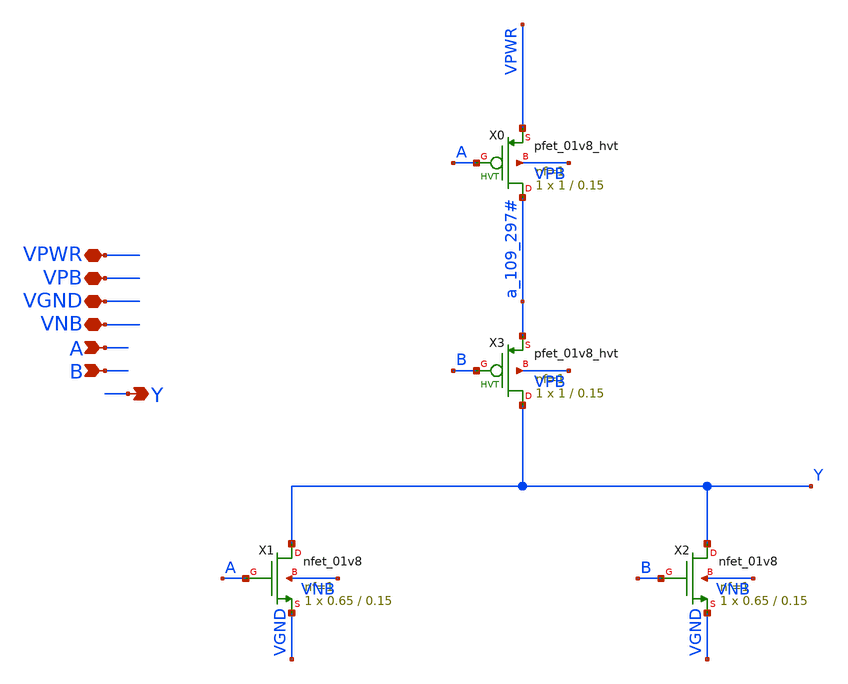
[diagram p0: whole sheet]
** sch_path: analog/xschem/sky130_fd_sc_hd__nor2_1.sch
**.subckt sky130_fd_sc_hd__nor2_1 A Y VNB VPB VPWR B VGND
*.ipin A
*.opin Y
*.iopin VNB
*.iopin VPB
*.iopin VPWR
*.ipin B
*.iopin VGND
XX1 Y A VGND VNB sky130_fd_pr__nfet_01v8 L=0.15 W=0.65 nf=1 ad='int((1 + 1)/2) * 0.65 / 1 * 0.29' as='int((1 + 2)/2) * 0.65 / 1 * 0.29'
+ pd='2*int((1 + 1)/2) * (0.65 / 1 + 0.29)' ps='2*int((1 + 2)/2) * (0.65 / 1 + 0.29)' nrd='0.29 / 0.65 '
+ nrs='0.29 / 0.65 ' sa=0 sb=0 sd=0 mult=1 m=1
XX2 Y B VGND VNB sky130_fd_pr__nfet_01v8 L=0.15 W=0.65 nf=1 ad='int((1 + 1)/2) * 0.65 / 1 * 0.29' as='int((1 + 2)/2) * 0.65 / 1 * 0.29'
+ pd='2*int((1 + 1)/2) * (0.65 / 1 + 0.29)' ps='2*int((1 + 2)/2) * (0.65 / 1 + 0.29)' nrd='0.29 / 0.65 '
+ nrs='0.29 / 0.65 ' sa=0 sb=0 sd=0 mult=1 m=1
XX3 Y B a_109_297# VPB sky130_fd_pr__pfet_01v8_hvt L=0.15 W=1 nf=1 ad='int((1 + 1)/2) * 1 / 1 * 0.29'
+ as='int((1 + 2)/2) * 1 / 1 * 0.29' pd='2*int((1 + 1)/2) * (1 / 1 + 0.29)' ps='2*int((1 + 2)/2) * (1 / 1 + 0.29)'
+ nrd='0.29 / 1 ' nrs='0.29 / 1 ' sa=0 sb=0 sd=0 mult=1 m=1
XX0 a_109_297# A VPWR VPB sky130_fd_pr__pfet_01v8_hvt L=0.15 W=1 nf=1 ad='int((1 + 1)/2) * 1 / 1 * 0.29'
+ as='int((1 + 2)/2) * 1 / 1 * 0.29' pd='2*int((1 + 1)/2) * (1 / 1 + 0.29)' ps='2*int((1 + 2)/2) * (1 / 1 + 0.29)'
+ nrd='0.29 / 1 ' nrs='0.29 / 1 ' sa=0 sb=0 sd=0 mult=1 m=1
**.ends
.end
